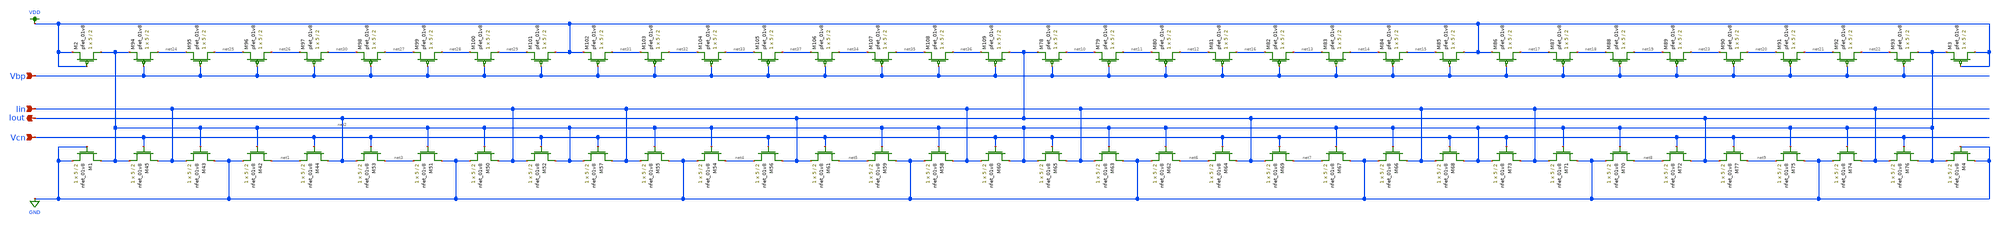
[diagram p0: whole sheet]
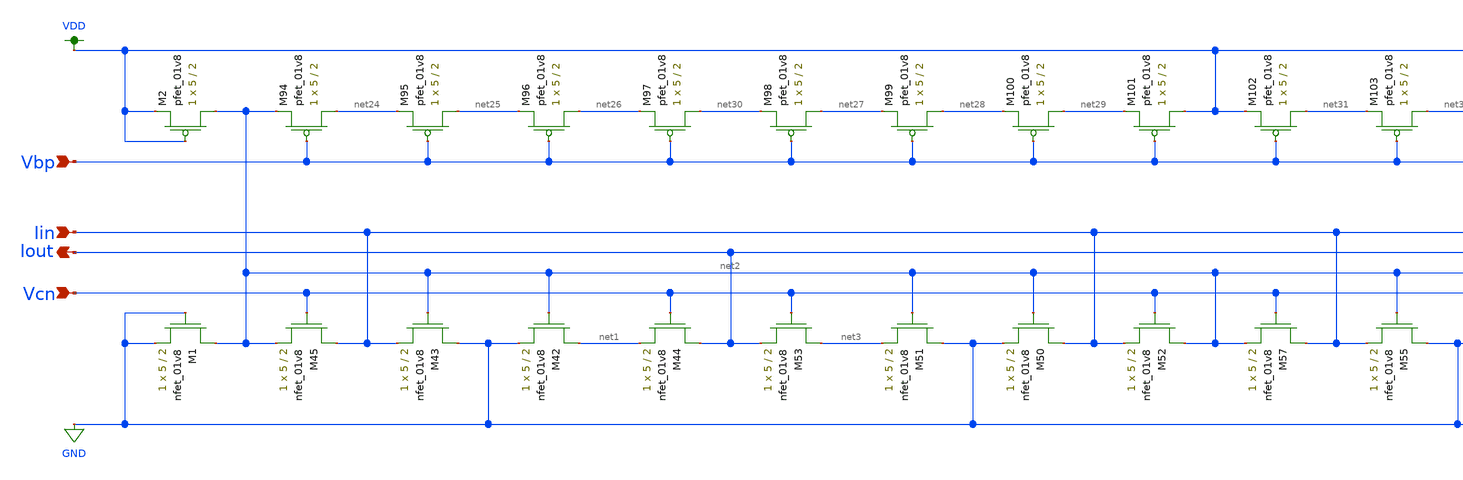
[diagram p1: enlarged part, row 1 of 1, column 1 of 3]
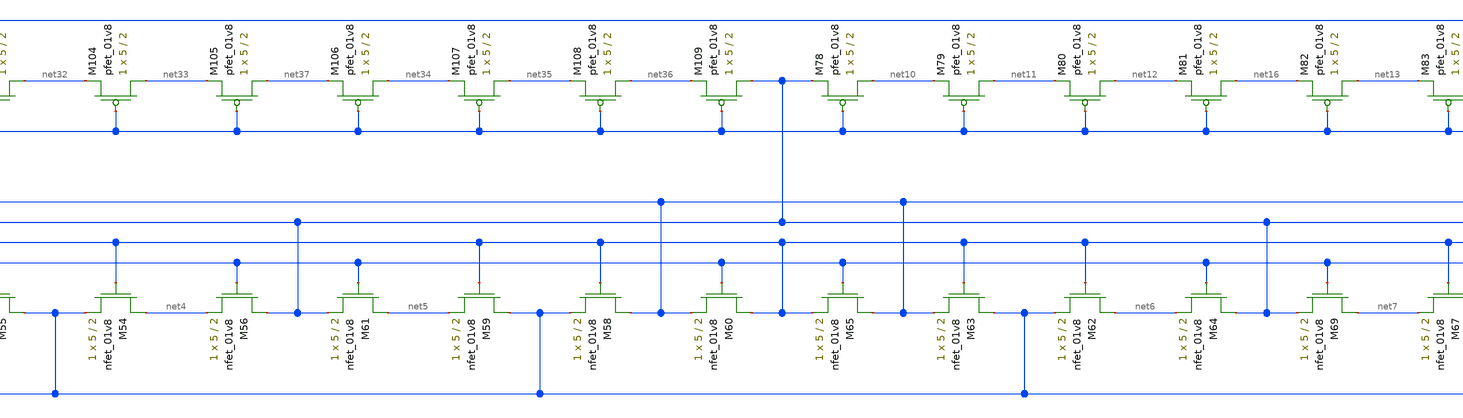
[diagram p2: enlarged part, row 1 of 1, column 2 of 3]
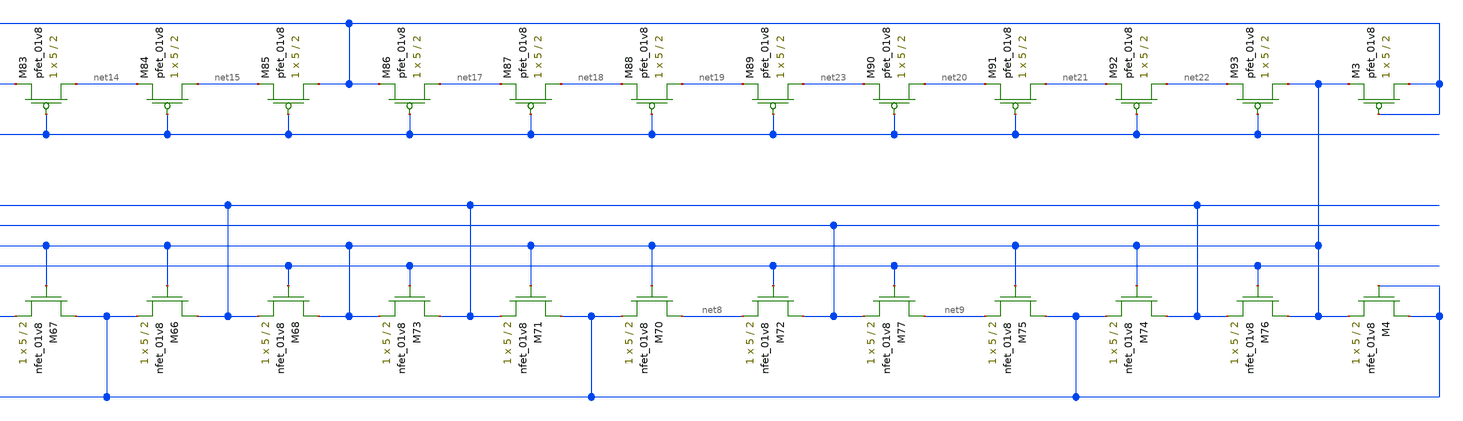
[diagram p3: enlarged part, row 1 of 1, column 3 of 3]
** sch_path: schematic/iout_mirror_LDS.sch
**.subckt iout_mirror_LDS Vcn Vbp Iout Iin
*.ipin Vcn
*.ipin Vbp
*.opin Iout
*.ipin Iin
XM42 net1 net2 GND GND sky130_fd_pr__nfet_01v8 L=2 W=5 nf=1 ad='int((nf+1)/2) * W/nf * 0.29' as='int((nf+2)/2) * W/nf * 0.29'
+ pd='2*int((nf+1)/2) * (W/nf + 0.29)' ps='2*int((nf+2)/2) * (W/nf + 0.29)' nrd='0.29 / W' nrs='0.29 / W'
+ sa=0 sb=0 sd=0 mult=1 m=1
XM43 GND net2 Iin GND sky130_fd_pr__nfet_01v8 L=2 W=5 nf=1 ad='int((nf+1)/2) * W/nf * 0.29' as='int((nf+2)/2) * W/nf * 0.29'
+ pd='2*int((nf+1)/2) * (W/nf + 0.29)' ps='2*int((nf+2)/2) * (W/nf + 0.29)' nrd='0.29 / W' nrs='0.29 / W'
+ sa=0 sb=0 sd=0 mult=1 m=1
XM44 Iout Vcn net1 GND sky130_fd_pr__nfet_01v8 L=2 W=5 nf=1 ad='int((nf+1)/2) * W/nf * 0.29' as='int((nf+2)/2) * W/nf * 0.29'
+ pd='2*int((nf+1)/2) * (W/nf + 0.29)' ps='2*int((nf+2)/2) * (W/nf + 0.29)' nrd='0.29 / W' nrs='0.29 / W'
+ sa=0 sb=0 sd=0 mult=1 m=1
XM45 Iin Vcn net2 GND sky130_fd_pr__nfet_01v8 L=2 W=5 nf=1 ad='int((nf+1)/2) * W/nf * 0.29' as='int((nf+2)/2) * W/nf * 0.29'
+ pd='2*int((nf+1)/2) * (W/nf + 0.29)' ps='2*int((nf+2)/2) * (W/nf + 0.29)' nrd='0.29 / W' nrs='0.29 / W'
+ sa=0 sb=0 sd=0 mult=1 m=1
XM50 Iin net2 GND GND sky130_fd_pr__nfet_01v8 L=2 W=5 nf=1 ad='int((nf+1)/2) * W/nf * 0.29' as='int((nf+2)/2) * W/nf * 0.29'
+ pd='2*int((nf+1)/2) * (W/nf + 0.29)' ps='2*int((nf+2)/2) * (W/nf + 0.29)' nrd='0.29 / W' nrs='0.29 / W'
+ sa=0 sb=0 sd=0 mult=1 m=1
XM51 GND net2 net3 GND sky130_fd_pr__nfet_01v8 L=2 W=5 nf=1 ad='int((nf+1)/2) * W/nf * 0.29' as='int((nf+2)/2) * W/nf * 0.29'
+ pd='2*int((nf+1)/2) * (W/nf + 0.29)' ps='2*int((nf+2)/2) * (W/nf + 0.29)' nrd='0.29 / W' nrs='0.29 / W'
+ sa=0 sb=0 sd=0 mult=1 m=1
XM52 net2 Vcn Iin GND sky130_fd_pr__nfet_01v8 L=2 W=5 nf=1 ad='int((nf+1)/2) * W/nf * 0.29' as='int((nf+2)/2) * W/nf * 0.29'
+ pd='2*int((nf+1)/2) * (W/nf + 0.29)' ps='2*int((nf+2)/2) * (W/nf + 0.29)' nrd='0.29 / W' nrs='0.29 / W'
+ sa=0 sb=0 sd=0 mult=1 m=1
XM53 net3 Vcn Iout GND sky130_fd_pr__nfet_01v8 L=2 W=5 nf=1 ad='int((nf+1)/2) * W/nf * 0.29' as='int((nf+2)/2) * W/nf * 0.29'
+ pd='2*int((nf+1)/2) * (W/nf + 0.29)' ps='2*int((nf+2)/2) * (W/nf + 0.29)' nrd='0.29 / W' nrs='0.29 / W'
+ sa=0 sb=0 sd=0 mult=1 m=1
XM54 net4 net2 GND GND sky130_fd_pr__nfet_01v8 L=2 W=5 nf=1 ad='int((nf+1)/2) * W/nf * 0.29' as='int((nf+2)/2) * W/nf * 0.29'
+ pd='2*int((nf+1)/2) * (W/nf + 0.29)' ps='2*int((nf+2)/2) * (W/nf + 0.29)' nrd='0.29 / W' nrs='0.29 / W'
+ sa=0 sb=0 sd=0 mult=1 m=1
XM55 GND net2 Iin GND sky130_fd_pr__nfet_01v8 L=2 W=5 nf=1 ad='int((nf+1)/2) * W/nf * 0.29' as='int((nf+2)/2) * W/nf * 0.29'
+ pd='2*int((nf+1)/2) * (W/nf + 0.29)' ps='2*int((nf+2)/2) * (W/nf + 0.29)' nrd='0.29 / W' nrs='0.29 / W'
+ sa=0 sb=0 sd=0 mult=1 m=1
XM56 Iout Vcn net4 GND sky130_fd_pr__nfet_01v8 L=2 W=5 nf=1 ad='int((nf+1)/2) * W/nf * 0.29' as='int((nf+2)/2) * W/nf * 0.29'
+ pd='2*int((nf+1)/2) * (W/nf + 0.29)' ps='2*int((nf+2)/2) * (W/nf + 0.29)' nrd='0.29 / W' nrs='0.29 / W'
+ sa=0 sb=0 sd=0 mult=1 m=1
XM57 Iin Vcn net2 GND sky130_fd_pr__nfet_01v8 L=2 W=5 nf=1 ad='int((nf+1)/2) * W/nf * 0.29' as='int((nf+2)/2) * W/nf * 0.29'
+ pd='2*int((nf+1)/2) * (W/nf + 0.29)' ps='2*int((nf+2)/2) * (W/nf + 0.29)' nrd='0.29 / W' nrs='0.29 / W'
+ sa=0 sb=0 sd=0 mult=1 m=1
XM58 Iin net2 GND GND sky130_fd_pr__nfet_01v8 L=2 W=5 nf=1 ad='int((nf+1)/2) * W/nf * 0.29' as='int((nf+2)/2) * W/nf * 0.29'
+ pd='2*int((nf+1)/2) * (W/nf + 0.29)' ps='2*int((nf+2)/2) * (W/nf + 0.29)' nrd='0.29 / W' nrs='0.29 / W'
+ sa=0 sb=0 sd=0 mult=1 m=1
XM59 GND net2 net5 GND sky130_fd_pr__nfet_01v8 L=2 W=5 nf=1 ad='int((nf+1)/2) * W/nf * 0.29' as='int((nf+2)/2) * W/nf * 0.29'
+ pd='2*int((nf+1)/2) * (W/nf + 0.29)' ps='2*int((nf+2)/2) * (W/nf + 0.29)' nrd='0.29 / W' nrs='0.29 / W'
+ sa=0 sb=0 sd=0 mult=1 m=1
XM60 net2 Vcn Iin GND sky130_fd_pr__nfet_01v8 L=2 W=5 nf=1 ad='int((nf+1)/2) * W/nf * 0.29' as='int((nf+2)/2) * W/nf * 0.29'
+ pd='2*int((nf+1)/2) * (W/nf + 0.29)' ps='2*int((nf+2)/2) * (W/nf + 0.29)' nrd='0.29 / W' nrs='0.29 / W'
+ sa=0 sb=0 sd=0 mult=1 m=1
XM61 net5 Vcn Iout GND sky130_fd_pr__nfet_01v8 L=2 W=5 nf=1 ad='int((nf+1)/2) * W/nf * 0.29' as='int((nf+2)/2) * W/nf * 0.29'
+ pd='2*int((nf+1)/2) * (W/nf + 0.29)' ps='2*int((nf+2)/2) * (W/nf + 0.29)' nrd='0.29 / W' nrs='0.29 / W'
+ sa=0 sb=0 sd=0 mult=1 m=1
XM62 net6 net2 GND GND sky130_fd_pr__nfet_01v8 L=2 W=5 nf=1 ad='int((nf+1)/2) * W/nf * 0.29' as='int((nf+2)/2) * W/nf * 0.29'
+ pd='2*int((nf+1)/2) * (W/nf + 0.29)' ps='2*int((nf+2)/2) * (W/nf + 0.29)' nrd='0.29 / W' nrs='0.29 / W'
+ sa=0 sb=0 sd=0 mult=1 m=1
XM63 GND net2 Iin GND sky130_fd_pr__nfet_01v8 L=2 W=5 nf=1 ad='int((nf+1)/2) * W/nf * 0.29' as='int((nf+2)/2) * W/nf * 0.29'
+ pd='2*int((nf+1)/2) * (W/nf + 0.29)' ps='2*int((nf+2)/2) * (W/nf + 0.29)' nrd='0.29 / W' nrs='0.29 / W'
+ sa=0 sb=0 sd=0 mult=1 m=1
XM64 Iout Vcn net6 GND sky130_fd_pr__nfet_01v8 L=2 W=5 nf=1 ad='int((nf+1)/2) * W/nf * 0.29' as='int((nf+2)/2) * W/nf * 0.29'
+ pd='2*int((nf+1)/2) * (W/nf + 0.29)' ps='2*int((nf+2)/2) * (W/nf + 0.29)' nrd='0.29 / W' nrs='0.29 / W'
+ sa=0 sb=0 sd=0 mult=1 m=1
XM65 Iin Vcn net2 GND sky130_fd_pr__nfet_01v8 L=2 W=5 nf=1 ad='int((nf+1)/2) * W/nf * 0.29' as='int((nf+2)/2) * W/nf * 0.29'
+ pd='2*int((nf+1)/2) * (W/nf + 0.29)' ps='2*int((nf+2)/2) * (W/nf + 0.29)' nrd='0.29 / W' nrs='0.29 / W'
+ sa=0 sb=0 sd=0 mult=1 m=1
XM66 Iin net2 GND GND sky130_fd_pr__nfet_01v8 L=2 W=5 nf=1 ad='int((nf+1)/2) * W/nf * 0.29' as='int((nf+2)/2) * W/nf * 0.29'
+ pd='2*int((nf+1)/2) * (W/nf + 0.29)' ps='2*int((nf+2)/2) * (W/nf + 0.29)' nrd='0.29 / W' nrs='0.29 / W'
+ sa=0 sb=0 sd=0 mult=1 m=1
XM67 GND net2 net7 GND sky130_fd_pr__nfet_01v8 L=2 W=5 nf=1 ad='int((nf+1)/2) * W/nf * 0.29' as='int((nf+2)/2) * W/nf * 0.29'
+ pd='2*int((nf+1)/2) * (W/nf + 0.29)' ps='2*int((nf+2)/2) * (W/nf + 0.29)' nrd='0.29 / W' nrs='0.29 / W'
+ sa=0 sb=0 sd=0 mult=1 m=1
XM68 net2 Vcn Iin GND sky130_fd_pr__nfet_01v8 L=2 W=5 nf=1 ad='int((nf+1)/2) * W/nf * 0.29' as='int((nf+2)/2) * W/nf * 0.29'
+ pd='2*int((nf+1)/2) * (W/nf + 0.29)' ps='2*int((nf+2)/2) * (W/nf + 0.29)' nrd='0.29 / W' nrs='0.29 / W'
+ sa=0 sb=0 sd=0 mult=1 m=1
XM69 net7 Vcn Iout GND sky130_fd_pr__nfet_01v8 L=2 W=5 nf=1 ad='int((nf+1)/2) * W/nf * 0.29' as='int((nf+2)/2) * W/nf * 0.29'
+ pd='2*int((nf+1)/2) * (W/nf + 0.29)' ps='2*int((nf+2)/2) * (W/nf + 0.29)' nrd='0.29 / W' nrs='0.29 / W'
+ sa=0 sb=0 sd=0 mult=1 m=1
XM70 net8 net2 GND GND sky130_fd_pr__nfet_01v8 L=2 W=5 nf=1 ad='int((nf+1)/2) * W/nf * 0.29' as='int((nf+2)/2) * W/nf * 0.29'
+ pd='2*int((nf+1)/2) * (W/nf + 0.29)' ps='2*int((nf+2)/2) * (W/nf + 0.29)' nrd='0.29 / W' nrs='0.29 / W'
+ sa=0 sb=0 sd=0 mult=1 m=1
XM71 GND net2 Iin GND sky130_fd_pr__nfet_01v8 L=2 W=5 nf=1 ad='int((nf+1)/2) * W/nf * 0.29' as='int((nf+2)/2) * W/nf * 0.29'
+ pd='2*int((nf+1)/2) * (W/nf + 0.29)' ps='2*int((nf+2)/2) * (W/nf + 0.29)' nrd='0.29 / W' nrs='0.29 / W'
+ sa=0 sb=0 sd=0 mult=1 m=1
XM72 Iout Vcn net8 GND sky130_fd_pr__nfet_01v8 L=2 W=5 nf=1 ad='int((nf+1)/2) * W/nf * 0.29' as='int((nf+2)/2) * W/nf * 0.29'
+ pd='2*int((nf+1)/2) * (W/nf + 0.29)' ps='2*int((nf+2)/2) * (W/nf + 0.29)' nrd='0.29 / W' nrs='0.29 / W'
+ sa=0 sb=0 sd=0 mult=1 m=1
XM73 Iin Vcn net2 GND sky130_fd_pr__nfet_01v8 L=2 W=5 nf=1 ad='int((nf+1)/2) * W/nf * 0.29' as='int((nf+2)/2) * W/nf * 0.29'
+ pd='2*int((nf+1)/2) * (W/nf + 0.29)' ps='2*int((nf+2)/2) * (W/nf + 0.29)' nrd='0.29 / W' nrs='0.29 / W'
+ sa=0 sb=0 sd=0 mult=1 m=1
XM74 Iin net2 GND GND sky130_fd_pr__nfet_01v8 L=2 W=5 nf=1 ad='int((nf+1)/2) * W/nf * 0.29' as='int((nf+2)/2) * W/nf * 0.29'
+ pd='2*int((nf+1)/2) * (W/nf + 0.29)' ps='2*int((nf+2)/2) * (W/nf + 0.29)' nrd='0.29 / W' nrs='0.29 / W'
+ sa=0 sb=0 sd=0 mult=1 m=1
XM75 GND net2 net9 GND sky130_fd_pr__nfet_01v8 L=2 W=5 nf=1 ad='int((nf+1)/2) * W/nf * 0.29' as='int((nf+2)/2) * W/nf * 0.29'
+ pd='2*int((nf+1)/2) * (W/nf + 0.29)' ps='2*int((nf+2)/2) * (W/nf + 0.29)' nrd='0.29 / W' nrs='0.29 / W'
+ sa=0 sb=0 sd=0 mult=1 m=1
XM76 net2 Vcn Iin GND sky130_fd_pr__nfet_01v8 L=2 W=5 nf=1 ad='int((nf+1)/2) * W/nf * 0.29' as='int((nf+2)/2) * W/nf * 0.29'
+ pd='2*int((nf+1)/2) * (W/nf + 0.29)' ps='2*int((nf+2)/2) * (W/nf + 0.29)' nrd='0.29 / W' nrs='0.29 / W'
+ sa=0 sb=0 sd=0 mult=1 m=1
XM77 net9 Vcn Iout GND sky130_fd_pr__nfet_01v8 L=2 W=5 nf=1 ad='int((nf+1)/2) * W/nf * 0.29' as='int((nf+2)/2) * W/nf * 0.29'
+ pd='2*int((nf+1)/2) * (W/nf + 0.29)' ps='2*int((nf+2)/2) * (W/nf + 0.29)' nrd='0.29 / W' nrs='0.29 / W'
+ sa=0 sb=0 sd=0 mult=1 m=1
XM78 net10 Vbp Iout VDD sky130_fd_pr__pfet_01v8 L=2 W=5 nf=1 ad='int((nf+1)/2) * W/nf * 0.29' as='int((nf+2)/2) * W/nf * 0.29'
+ pd='2*int((nf+1)/2) * (W/nf + 0.29)' ps='2*int((nf+2)/2) * (W/nf + 0.29)' nrd='0.29 / W' nrs='0.29 / W'
+ sa=0 sb=0 sd=0 mult=1 m=1
XM79 net11 Vbp net10 VDD sky130_fd_pr__pfet_01v8 L=2 W=5 nf=1 ad='int((nf+1)/2) * W/nf * 0.29' as='int((nf+2)/2) * W/nf * 0.29'
+ pd='2*int((nf+1)/2) * (W/nf + 0.29)' ps='2*int((nf+2)/2) * (W/nf + 0.29)' nrd='0.29 / W' nrs='0.29 / W'
+ sa=0 sb=0 sd=0 mult=1 m=1
XM80 net12 Vbp net11 VDD sky130_fd_pr__pfet_01v8 L=2 W=5 nf=1 ad='int((nf+1)/2) * W/nf * 0.29' as='int((nf+2)/2) * W/nf * 0.29'
+ pd='2*int((nf+1)/2) * (W/nf + 0.29)' ps='2*int((nf+2)/2) * (W/nf + 0.29)' nrd='0.29 / W' nrs='0.29 / W'
+ sa=0 sb=0 sd=0 mult=1 m=1
XM81 net16 Vbp net12 VDD sky130_fd_pr__pfet_01v8 L=2 W=5 nf=1 ad='int((nf+1)/2) * W/nf * 0.29' as='int((nf+2)/2) * W/nf * 0.29'
+ pd='2*int((nf+1)/2) * (W/nf + 0.29)' ps='2*int((nf+2)/2) * (W/nf + 0.29)' nrd='0.29 / W' nrs='0.29 / W'
+ sa=0 sb=0 sd=0 mult=1 m=1
XM82 net13 Vbp net16 VDD sky130_fd_pr__pfet_01v8 L=2 W=5 nf=1 ad='int((nf+1)/2) * W/nf * 0.29' as='int((nf+2)/2) * W/nf * 0.29'
+ pd='2*int((nf+1)/2) * (W/nf + 0.29)' ps='2*int((nf+2)/2) * (W/nf + 0.29)' nrd='0.29 / W' nrs='0.29 / W'
+ sa=0 sb=0 sd=0 mult=1 m=1
XM83 net14 Vbp net13 VDD sky130_fd_pr__pfet_01v8 L=2 W=5 nf=1 ad='int((nf+1)/2) * W/nf * 0.29' as='int((nf+2)/2) * W/nf * 0.29'
+ pd='2*int((nf+1)/2) * (W/nf + 0.29)' ps='2*int((nf+2)/2) * (W/nf + 0.29)' nrd='0.29 / W' nrs='0.29 / W'
+ sa=0 sb=0 sd=0 mult=1 m=1
XM84 net15 Vbp net14 VDD sky130_fd_pr__pfet_01v8 L=2 W=5 nf=1 ad='int((nf+1)/2) * W/nf * 0.29' as='int((nf+2)/2) * W/nf * 0.29'
+ pd='2*int((nf+1)/2) * (W/nf + 0.29)' ps='2*int((nf+2)/2) * (W/nf + 0.29)' nrd='0.29 / W' nrs='0.29 / W'
+ sa=0 sb=0 sd=0 mult=1 m=1
XM85 VDD Vbp net15 VDD sky130_fd_pr__pfet_01v8 L=2 W=5 nf=1 ad='int((nf+1)/2) * W/nf * 0.29' as='int((nf+2)/2) * W/nf * 0.29'
+ pd='2*int((nf+1)/2) * (W/nf + 0.29)' ps='2*int((nf+2)/2) * (W/nf + 0.29)' nrd='0.29 / W' nrs='0.29 / W'
+ sa=0 sb=0 sd=0 mult=1 m=1
XM86 net17 Vbp VDD VDD sky130_fd_pr__pfet_01v8 L=2 W=5 nf=1 ad='int((nf+1)/2) * W/nf * 0.29' as='int((nf+2)/2) * W/nf * 0.29'
+ pd='2*int((nf+1)/2) * (W/nf + 0.29)' ps='2*int((nf+2)/2) * (W/nf + 0.29)' nrd='0.29 / W' nrs='0.29 / W'
+ sa=0 sb=0 sd=0 mult=1 m=1
XM87 net18 Vbp net17 VDD sky130_fd_pr__pfet_01v8 L=2 W=5 nf=1 ad='int((nf+1)/2) * W/nf * 0.29' as='int((nf+2)/2) * W/nf * 0.29'
+ pd='2*int((nf+1)/2) * (W/nf + 0.29)' ps='2*int((nf+2)/2) * (W/nf + 0.29)' nrd='0.29 / W' nrs='0.29 / W'
+ sa=0 sb=0 sd=0 mult=1 m=1
XM88 net19 Vbp net18 VDD sky130_fd_pr__pfet_01v8 L=2 W=5 nf=1 ad='int((nf+1)/2) * W/nf * 0.29' as='int((nf+2)/2) * W/nf * 0.29'
+ pd='2*int((nf+1)/2) * (W/nf + 0.29)' ps='2*int((nf+2)/2) * (W/nf + 0.29)' nrd='0.29 / W' nrs='0.29 / W'
+ sa=0 sb=0 sd=0 mult=1 m=1
XM89 net23 Vbp net19 VDD sky130_fd_pr__pfet_01v8 L=2 W=5 nf=1 ad='int((nf+1)/2) * W/nf * 0.29' as='int((nf+2)/2) * W/nf * 0.29'
+ pd='2*int((nf+1)/2) * (W/nf + 0.29)' ps='2*int((nf+2)/2) * (W/nf + 0.29)' nrd='0.29 / W' nrs='0.29 / W'
+ sa=0 sb=0 sd=0 mult=1 m=1
XM90 net20 Vbp net23 VDD sky130_fd_pr__pfet_01v8 L=2 W=5 nf=1 ad='int((nf+1)/2) * W/nf * 0.29' as='int((nf+2)/2) * W/nf * 0.29'
+ pd='2*int((nf+1)/2) * (W/nf + 0.29)' ps='2*int((nf+2)/2) * (W/nf + 0.29)' nrd='0.29 / W' nrs='0.29 / W'
+ sa=0 sb=0 sd=0 mult=1 m=1
XM91 net21 Vbp net20 VDD sky130_fd_pr__pfet_01v8 L=2 W=5 nf=1 ad='int((nf+1)/2) * W/nf * 0.29' as='int((nf+2)/2) * W/nf * 0.29'
+ pd='2*int((nf+1)/2) * (W/nf + 0.29)' ps='2*int((nf+2)/2) * (W/nf + 0.29)' nrd='0.29 / W' nrs='0.29 / W'
+ sa=0 sb=0 sd=0 mult=1 m=1
XM92 net22 Vbp net21 VDD sky130_fd_pr__pfet_01v8 L=2 W=5 nf=1 ad='int((nf+1)/2) * W/nf * 0.29' as='int((nf+2)/2) * W/nf * 0.29'
+ pd='2*int((nf+1)/2) * (W/nf + 0.29)' ps='2*int((nf+2)/2) * (W/nf + 0.29)' nrd='0.29 / W' nrs='0.29 / W'
+ sa=0 sb=0 sd=0 mult=1 m=1
XM93 net2 Vbp net22 VDD sky130_fd_pr__pfet_01v8 L=2 W=5 nf=1 ad='int((nf+1)/2) * W/nf * 0.29' as='int((nf+2)/2) * W/nf * 0.29'
+ pd='2*int((nf+1)/2) * (W/nf + 0.29)' ps='2*int((nf+2)/2) * (W/nf + 0.29)' nrd='0.29 / W' nrs='0.29 / W'
+ sa=0 sb=0 sd=0 mult=1 m=1
XM94 net24 Vbp net2 VDD sky130_fd_pr__pfet_01v8 L=2 W=5 nf=1 ad='int((nf+1)/2) * W/nf * 0.29' as='int((nf+2)/2) * W/nf * 0.29'
+ pd='2*int((nf+1)/2) * (W/nf + 0.29)' ps='2*int((nf+2)/2) * (W/nf + 0.29)' nrd='0.29 / W' nrs='0.29 / W'
+ sa=0 sb=0 sd=0 mult=1 m=1
XM95 net25 Vbp net24 VDD sky130_fd_pr__pfet_01v8 L=2 W=5 nf=1 ad='int((nf+1)/2) * W/nf * 0.29' as='int((nf+2)/2) * W/nf * 0.29'
+ pd='2*int((nf+1)/2) * (W/nf + 0.29)' ps='2*int((nf+2)/2) * (W/nf + 0.29)' nrd='0.29 / W' nrs='0.29 / W'
+ sa=0 sb=0 sd=0 mult=1 m=1
XM96 net26 Vbp net25 VDD sky130_fd_pr__pfet_01v8 L=2 W=5 nf=1 ad='int((nf+1)/2) * W/nf * 0.29' as='int((nf+2)/2) * W/nf * 0.29'
+ pd='2*int((nf+1)/2) * (W/nf + 0.29)' ps='2*int((nf+2)/2) * (W/nf + 0.29)' nrd='0.29 / W' nrs='0.29 / W'
+ sa=0 sb=0 sd=0 mult=1 m=1
XM97 net30 Vbp net26 VDD sky130_fd_pr__pfet_01v8 L=2 W=5 nf=1 ad='int((nf+1)/2) * W/nf * 0.29' as='int((nf+2)/2) * W/nf * 0.29'
+ pd='2*int((nf+1)/2) * (W/nf + 0.29)' ps='2*int((nf+2)/2) * (W/nf + 0.29)' nrd='0.29 / W' nrs='0.29 / W'
+ sa=0 sb=0 sd=0 mult=1 m=1
XM98 net27 Vbp net30 VDD sky130_fd_pr__pfet_01v8 L=2 W=5 nf=1 ad='int((nf+1)/2) * W/nf * 0.29' as='int((nf+2)/2) * W/nf * 0.29'
+ pd='2*int((nf+1)/2) * (W/nf + 0.29)' ps='2*int((nf+2)/2) * (W/nf + 0.29)' nrd='0.29 / W' nrs='0.29 / W'
+ sa=0 sb=0 sd=0 mult=1 m=1
XM99 net28 Vbp net27 VDD sky130_fd_pr__pfet_01v8 L=2 W=5 nf=1 ad='int((nf+1)/2) * W/nf * 0.29' as='int((nf+2)/2) * W/nf * 0.29'
+ pd='2*int((nf+1)/2) * (W/nf + 0.29)' ps='2*int((nf+2)/2) * (W/nf + 0.29)' nrd='0.29 / W' nrs='0.29 / W'
+ sa=0 sb=0 sd=0 mult=1 m=1
XM100 net29 Vbp net28 VDD sky130_fd_pr__pfet_01v8 L=2 W=5 nf=1 ad='int((nf+1)/2) * W/nf * 0.29' as='int((nf+2)/2) * W/nf * 0.29'
+ pd='2*int((nf+1)/2) * (W/nf + 0.29)' ps='2*int((nf+2)/2) * (W/nf + 0.29)' nrd='0.29 / W' nrs='0.29 / W'
+ sa=0 sb=0 sd=0 mult=1 m=1
XM101 VDD Vbp net29 VDD sky130_fd_pr__pfet_01v8 L=2 W=5 nf=1 ad='int((nf+1)/2) * W/nf * 0.29' as='int((nf+2)/2) * W/nf * 0.29'
+ pd='2*int((nf+1)/2) * (W/nf + 0.29)' ps='2*int((nf+2)/2) * (W/nf + 0.29)' nrd='0.29 / W' nrs='0.29 / W'
+ sa=0 sb=0 sd=0 mult=1 m=1
XM102 net31 Vbp VDD VDD sky130_fd_pr__pfet_01v8 L=2 W=5 nf=1 ad='int((nf+1)/2) * W/nf * 0.29' as='int((nf+2)/2) * W/nf * 0.29'
+ pd='2*int((nf+1)/2) * (W/nf + 0.29)' ps='2*int((nf+2)/2) * (W/nf + 0.29)' nrd='0.29 / W' nrs='0.29 / W'
+ sa=0 sb=0 sd=0 mult=1 m=1
XM103 net32 Vbp net31 VDD sky130_fd_pr__pfet_01v8 L=2 W=5 nf=1 ad='int((nf+1)/2) * W/nf * 0.29' as='int((nf+2)/2) * W/nf * 0.29'
+ pd='2*int((nf+1)/2) * (W/nf + 0.29)' ps='2*int((nf+2)/2) * (W/nf + 0.29)' nrd='0.29 / W' nrs='0.29 / W'
+ sa=0 sb=0 sd=0 mult=1 m=1
XM104 net33 Vbp net32 VDD sky130_fd_pr__pfet_01v8 L=2 W=5 nf=1 ad='int((nf+1)/2) * W/nf * 0.29' as='int((nf+2)/2) * W/nf * 0.29'
+ pd='2*int((nf+1)/2) * (W/nf + 0.29)' ps='2*int((nf+2)/2) * (W/nf + 0.29)' nrd='0.29 / W' nrs='0.29 / W'
+ sa=0 sb=0 sd=0 mult=1 m=1
XM105 net37 Vbp net33 VDD sky130_fd_pr__pfet_01v8 L=2 W=5 nf=1 ad='int((nf+1)/2) * W/nf * 0.29' as='int((nf+2)/2) * W/nf * 0.29'
+ pd='2*int((nf+1)/2) * (W/nf + 0.29)' ps='2*int((nf+2)/2) * (W/nf + 0.29)' nrd='0.29 / W' nrs='0.29 / W'
+ sa=0 sb=0 sd=0 mult=1 m=1
XM106 net34 Vbp net37 VDD sky130_fd_pr__pfet_01v8 L=2 W=5 nf=1 ad='int((nf+1)/2) * W/nf * 0.29' as='int((nf+2)/2) * W/nf * 0.29'
+ pd='2*int((nf+1)/2) * (W/nf + 0.29)' ps='2*int((nf+2)/2) * (W/nf + 0.29)' nrd='0.29 / W' nrs='0.29 / W'
+ sa=0 sb=0 sd=0 mult=1 m=1
XM107 net35 Vbp net34 VDD sky130_fd_pr__pfet_01v8 L=2 W=5 nf=1 ad='int((nf+1)/2) * W/nf * 0.29' as='int((nf+2)/2) * W/nf * 0.29'
+ pd='2*int((nf+1)/2) * (W/nf + 0.29)' ps='2*int((nf+2)/2) * (W/nf + 0.29)' nrd='0.29 / W' nrs='0.29 / W'
+ sa=0 sb=0 sd=0 mult=1 m=1
XM108 net36 Vbp net35 VDD sky130_fd_pr__pfet_01v8 L=2 W=5 nf=1 ad='int((nf+1)/2) * W/nf * 0.29' as='int((nf+2)/2) * W/nf * 0.29'
+ pd='2*int((nf+1)/2) * (W/nf + 0.29)' ps='2*int((nf+2)/2) * (W/nf + 0.29)' nrd='0.29 / W' nrs='0.29 / W'
+ sa=0 sb=0 sd=0 mult=1 m=1
XM109 Iout Vbp net36 VDD sky130_fd_pr__pfet_01v8 L=2 W=5 nf=1 ad='int((nf+1)/2) * W/nf * 0.29' as='int((nf+2)/2) * W/nf * 0.29'
+ pd='2*int((nf+1)/2) * (W/nf + 0.29)' ps='2*int((nf+2)/2) * (W/nf + 0.29)' nrd='0.29 / W' nrs='0.29 / W'
+ sa=0 sb=0 sd=0 mult=1 m=1
XM1 net2 GND GND GND sky130_fd_pr__nfet_01v8 L=2 W=5 nf=1 ad='int((nf+1)/2) * W/nf * 0.29' as='int((nf+2)/2) * W/nf * 0.29'
+ pd='2*int((nf+1)/2) * (W/nf + 0.29)' ps='2*int((nf+2)/2) * (W/nf + 0.29)' nrd='0.29 / W' nrs='0.29 / W'
+ sa=0 sb=0 sd=0 mult=1 m=1
XM2 net2 VDD VDD VDD sky130_fd_pr__pfet_01v8 L=2 W=5 nf=1 ad='int((nf+1)/2) * W/nf * 0.29' as='int((nf+2)/2) * W/nf * 0.29'
+ pd='2*int((nf+1)/2) * (W/nf + 0.29)' ps='2*int((nf+2)/2) * (W/nf + 0.29)' nrd='0.29 / W' nrs='0.29 / W'
+ sa=0 sb=0 sd=0 mult=1 m=1
XM3 VDD VDD net2 VDD sky130_fd_pr__pfet_01v8 L=2 W=5 nf=1 ad='int((nf+1)/2) * W/nf * 0.29' as='int((nf+2)/2) * W/nf * 0.29'
+ pd='2*int((nf+1)/2) * (W/nf + 0.29)' ps='2*int((nf+2)/2) * (W/nf + 0.29)' nrd='0.29 / W' nrs='0.29 / W'
+ sa=0 sb=0 sd=0 mult=1 m=1
XM4 GND GND net2 GND sky130_fd_pr__nfet_01v8 L=2 W=5 nf=1 ad='int((nf+1)/2) * W/nf * 0.29' as='int((nf+2)/2) * W/nf * 0.29'
+ pd='2*int((nf+1)/2) * (W/nf + 0.29)' ps='2*int((nf+2)/2) * (W/nf + 0.29)' nrd='0.29 / W' nrs='0.29 / W'
+ sa=0 sb=0 sd=0 mult=1 m=1
**.ends
.GLOBAL VDD
.GLOBAL GND
.end
